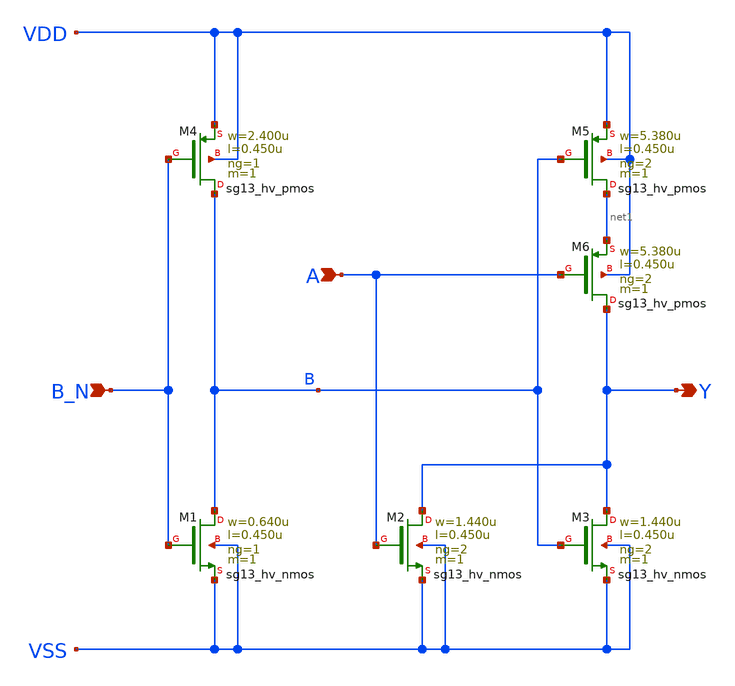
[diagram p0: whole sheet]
** sch_path: ihp-sg13g2/libs.ref/sg13g2_stdcell_hv/sch/xschem/sg13g2_hv_nor2b_2.sch
* Copyright 2023 IHP PDK Authors
* Licensed under the Apache License, Version 2.0 (the "License");
* you may not use this file except in compliance with the License.
* You may obtain a copy of the License at
* https://www.apache.org/licenses/LICENSE-2.0
* Unless required by applicable law or agreed to in writing, software
* distributed under the License is distributed on an "AS IS" BASIS,
* WITHOUT WARRANTIES OR CONDITIONS OF ANY KIND, either express or implied.
* See the License for the specific language governing permissions and
* limitations under the License.
**.subckt sg13g2_hv_nor2b_2 Y B_N A
*.opin Y
*.ipin B_N
*.ipin A
XM1 B B_N VSS VSS sg13_hv_nmos w=0.640u l=0.450u ng=1 m=1 mm_ok=1
XM2 Y A VSS VSS sg13_hv_nmos w=1.440u l=0.450u ng=2 m=1 mm_ok=1
XM3 Y B VSS VSS sg13_hv_nmos w=1.440u l=0.450u ng=2 m=1 mm_ok=1
XM4 B B_N VDD VDD sg13_hv_pmos w=2.400u l=0.450u ng=1 m=1 mm_ok=1
XM5 net1 B VDD VDD sg13_hv_pmos w=5.380u l=0.450u ng=2 m=1 mm_ok=1
XM6 Y A net1 VDD sg13_hv_pmos w=5.380u l=0.450u ng=2 m=1 mm_ok=1
**.ends
.end
